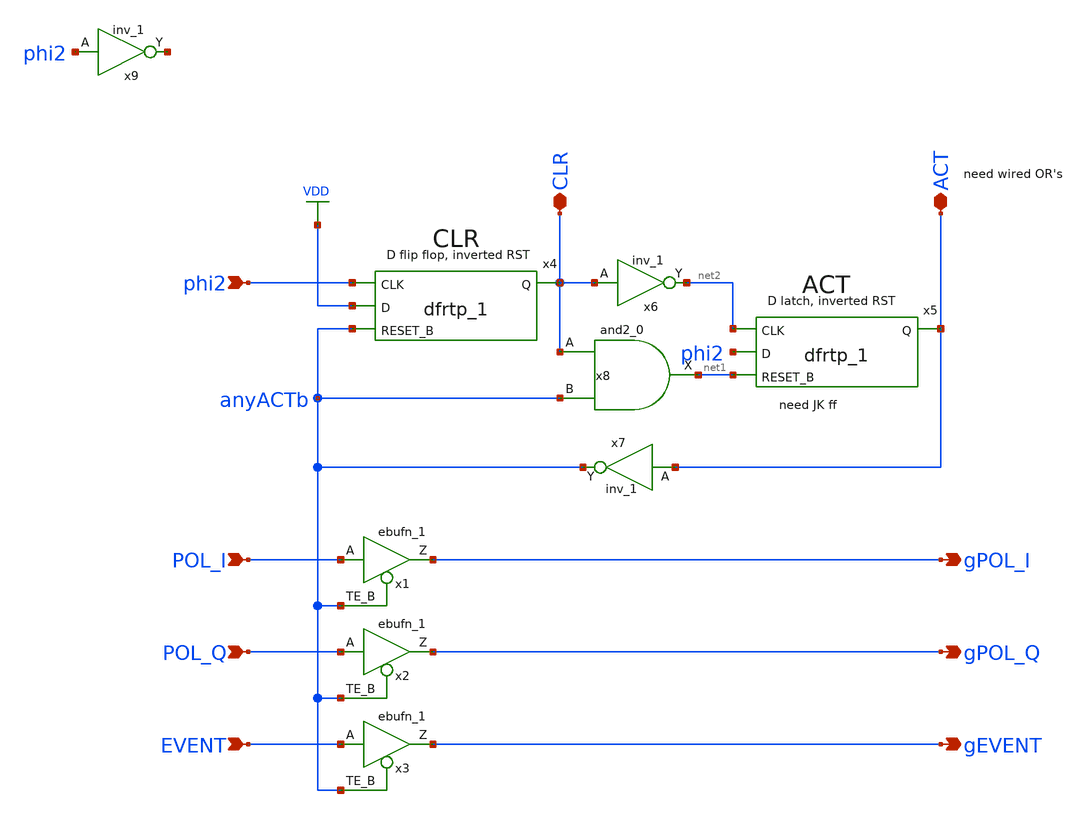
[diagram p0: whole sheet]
** sch_path: xschem/readout/CLR_ACT.sch
**.subckt CLR_ACT POL_I POL_Q EVENT gPOL_I gPOL_Q gEVENT phi2 CLR ACT
*.ipin POL_I
*.ipin POL_Q
*.ipin EVENT
*.opin gPOL_I
*.opin gPOL_Q
*.opin gEVENT
*.ipin phi2
*.iopin CLR
*.iopin ACT
x1 POL_I anyACTb gnd gnd vdd vdd gPOL_I sky130_fd_sc_lp__ebufn_1
x4 phi2 VDD anyACTb gnd gnd vdd vdd CLR sky130_fd_sc_lp__dfrtp_1
x7 ACT gnd gnd vdd vdd anyACTb sky130_fd_sc_lp__inv_1
x8 CLR anyACTb gnd gnd vdd vdd net1 sky130_fd_sc_lp__and2_0
x6 CLR gnd gnd vdd vdd net2 sky130_fd_sc_lp__inv_1
x2 POL_Q anyACTb gnd gnd vdd vdd gPOL_Q sky130_fd_sc_lp__ebufn_1
x3 EVENT anyACTb gnd gnd vdd vdd gEVENT sky130_fd_sc_lp__ebufn_1
x5 net2 phi2 net1 gnd gnd vdd vdd ACT sky130_fd_sc_lp__dfrtp_1
x9 phi2 gnd gnd vdd vdd net3 sky130_fd_sc_lp__inv_1
**.ends
.GLOBAL VDD
.end
